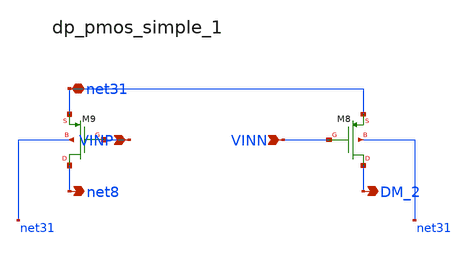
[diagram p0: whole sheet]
** sch_path: analog-db/raw/amp_017_tan_clia/hier/blocks/dp_pmos_simple_1.sch
**.subckt dp_pmos_simple_1 VINP VINN net31 net8 DM_2
*.ipin VINP
*.ipin VINN
*.iopin net31
*.opin net8
*.opin DM_2
XM8 DM_2 VINN net31 net31 sg13_lv_pmos w=x_dut_xm8_w l=x_dut_xm8_l ng=1 m=x_dut_xm8_m
XM9 net8 VINP net31 net31 sg13_lv_pmos w=x_dut_xm9_w l=x_dut_xm9_l ng=1 m=x_dut_xm9_m
**.ends
.end
